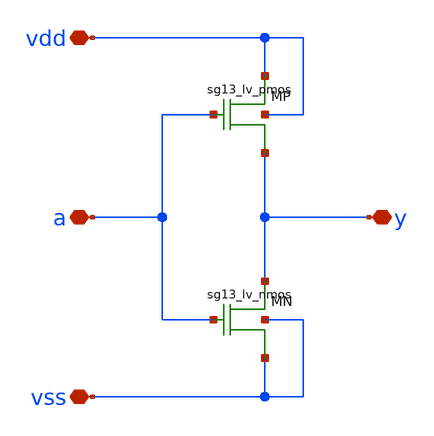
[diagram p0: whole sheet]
** sch_path: xschem/logic_gates/INVLVW.sch
**.subckt INVLVW vdd vss y a
*.iopin vdd
*.iopin vss
*.iopin y
*.iopin a
XMP vdd a y vdd sg13_lv_pmos w=0.3u l=0.3u ng=1 m=1
XMN y a vss vss sg13_lv_nmos w=0.3u l=0.3u ng=1 m=1
**.ends
.end
